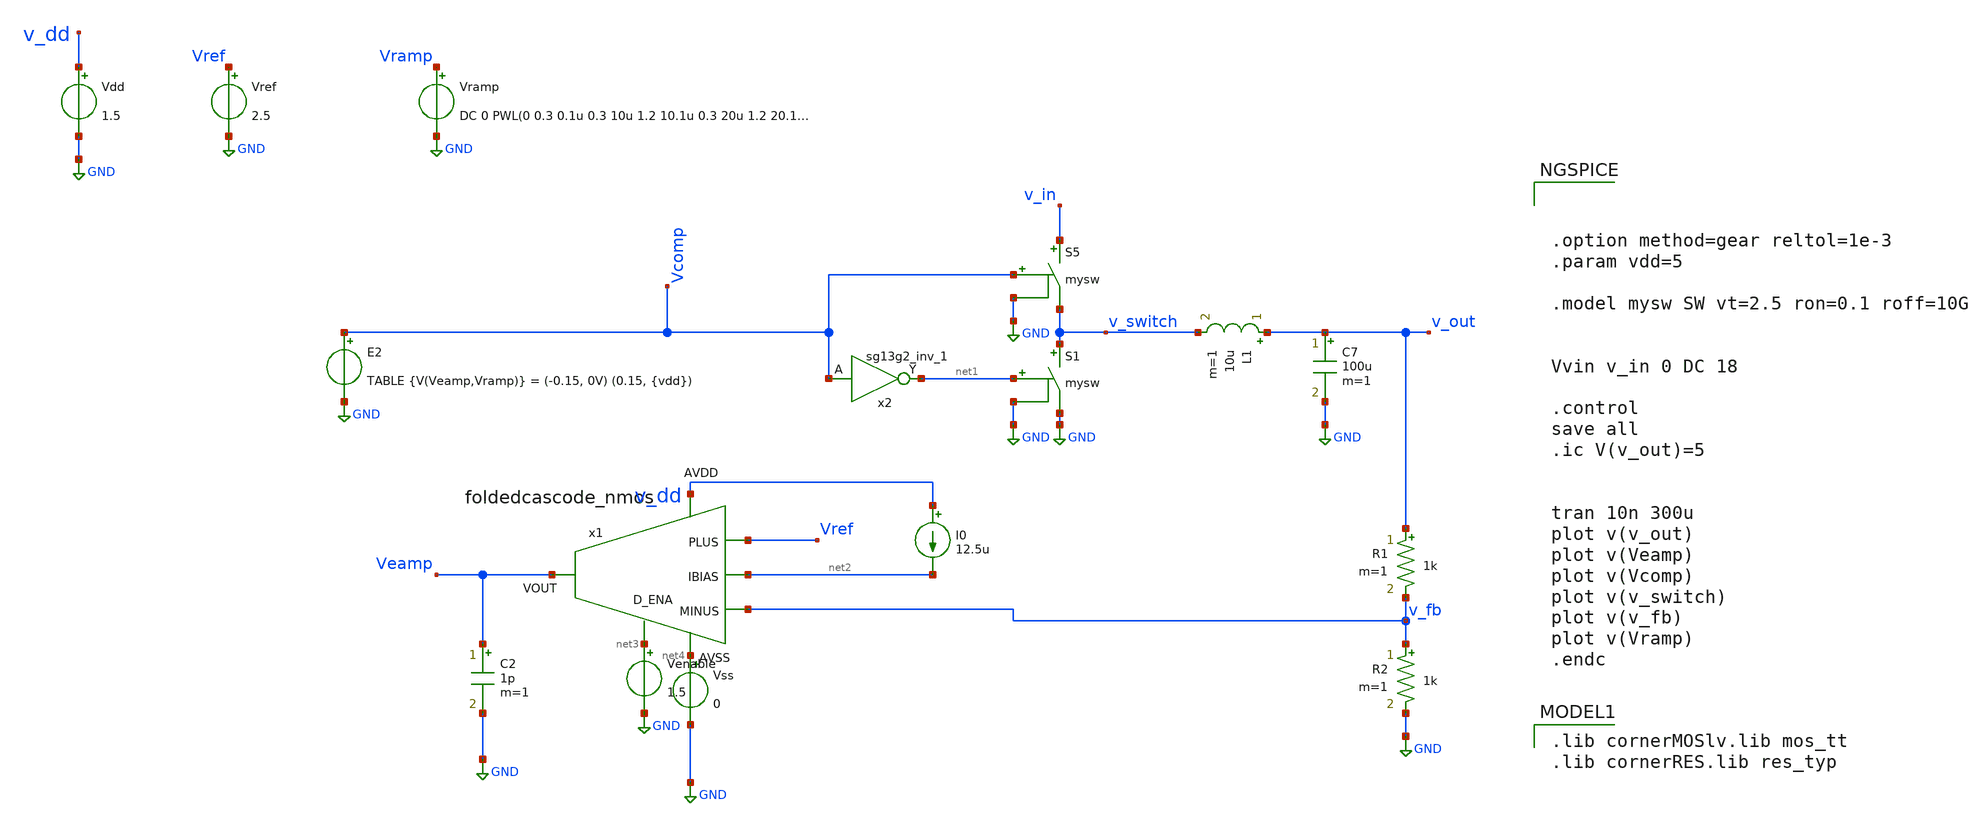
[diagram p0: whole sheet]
** sch_path: Designs/ideal_circuits/ideal_dcdc.sch
* (c) 2025 Thesis_HP, Apache-2.0 license
**.subckt ideal_dcdc
Vramp Vramp GND DC 0 PWL(0 0.3 0.1u 0.3 10u 1.2 10.1u 0.3 20u 1.2 20.1u 0.3 30u 1.2 30.1u 0.3 40u
+ 1.2 40.1u 0.3 50u 1.2 50.1u 0.3 60u 1.2 60.1u 0.3 70u 1.2 70.1u 0.3 80u 1.2 80.1u 0.3 90u 1.2 90.1u 0.3
+ 100u 1.2 100.1u 0.3 110u 1.2 110.1u 0.3 120u 1.2 120.1u 0.3 130u 1.2 130.1u 0.3 140u 1.2 140.1u 0.3 150u
+ 1.2 150.1u 0.3 160u 1.2 160.1u 0.3 170u 1.2 170.1u 0.3 180u 1.2 180.1u 0.3 190u 1.2 190.1u 0.3 200u 1.2
+ 200.1u 0.3 210u 1.2 210.1u 0.3 220u 1.2 220.1u 0.3 230u 1.2 230.1u 0.3 240u 1.2 240.1u 0.3 250u 1.2 250.1u
+ 0.3 260u 1.2 260.1u 0.3 270u 1.2 270.1u 0.3 280u 1.2 280.1u 0.3 290u 1.2 290.1u 0.3 300u 1.2)
S5 v_in v_switch Vcomp GND mysw
S1 v_switch GND net1 GND mysw
L1 v_out v_switch 10u m=1
C7 v_out GND 100u m=1
R1 v_out v_fb 1k m=1
R2 v_fb GND 1k m=1
Vref Vref GND 2.5
x2 net1 Vcomp 1.5 0 sg13g2_inv_1
E2 Vcomp GND TABLE {V(Veamp,Vramp)} = (-0.15, 0V) (0.15, {vdd})
x1 v_dd net2 Veamp v_fb Vref net3 net4 foldedcascode_nmos
Vdd v_dd GND 1.5
Vss net4 GND 0
Venable net3 GND 1.5
I0 v_dd net2 12.5u
C2 Veamp GND 1p m=1
**** begin user architecture code



.option method=gear reltol=1e-3
.param vdd=5

.model mysw SW vt=2.5 ron=0.1 roff=10G


Vvin v_in 0 DC 18

.control
save all
.ic V(v_out)=5


tran 10n 300u
plot v(v_out)
plot v(Veamp)
plot v(Vcomp)
plot v(v_switch)
plot v(v_fb)
plot v(Vramp)
.endc


 .lib cornerMOSlv.lib mos_tt
.lib cornerRES.lib res_typ


.lib $::SG13G2_MODELS/cornerMOSlv.lib mos_tt
.lib $::SG13G2_MODELS/cornerRES.lib res_typ
.inc /foss/pdks/ihp-sg13g2/libs.ref/sg13g2_stdcell/spice/sg13g2_stdcell.spice

**** end user architecture code
**.ends

* expanding   symbol:  sg13g2_stdcells/sg13g2_inv_1.sym # of pins=2
** sym_path: sg13g2_stdcells/sg13g2_inv_1.sym
** sch_path: sg13g2_stdcells/sg13g2_inv_1.sch
.subckt sg13g2_inv_1 Y A VDD VSS
*.opin Y
*.ipin A
*.iopin VDD
*.iopin VSS
XM1 Y A VSS VSS sg13_lv_nmos w=740.00n l=130.00n ng=1 m=1 mm_ok=1
XM2 Y A VDD VDD sg13_lv_pmos w=1.12u l=130.00n ng=1 m=1 mm_ok=1
.ends

.GLOBAL GND
.end
